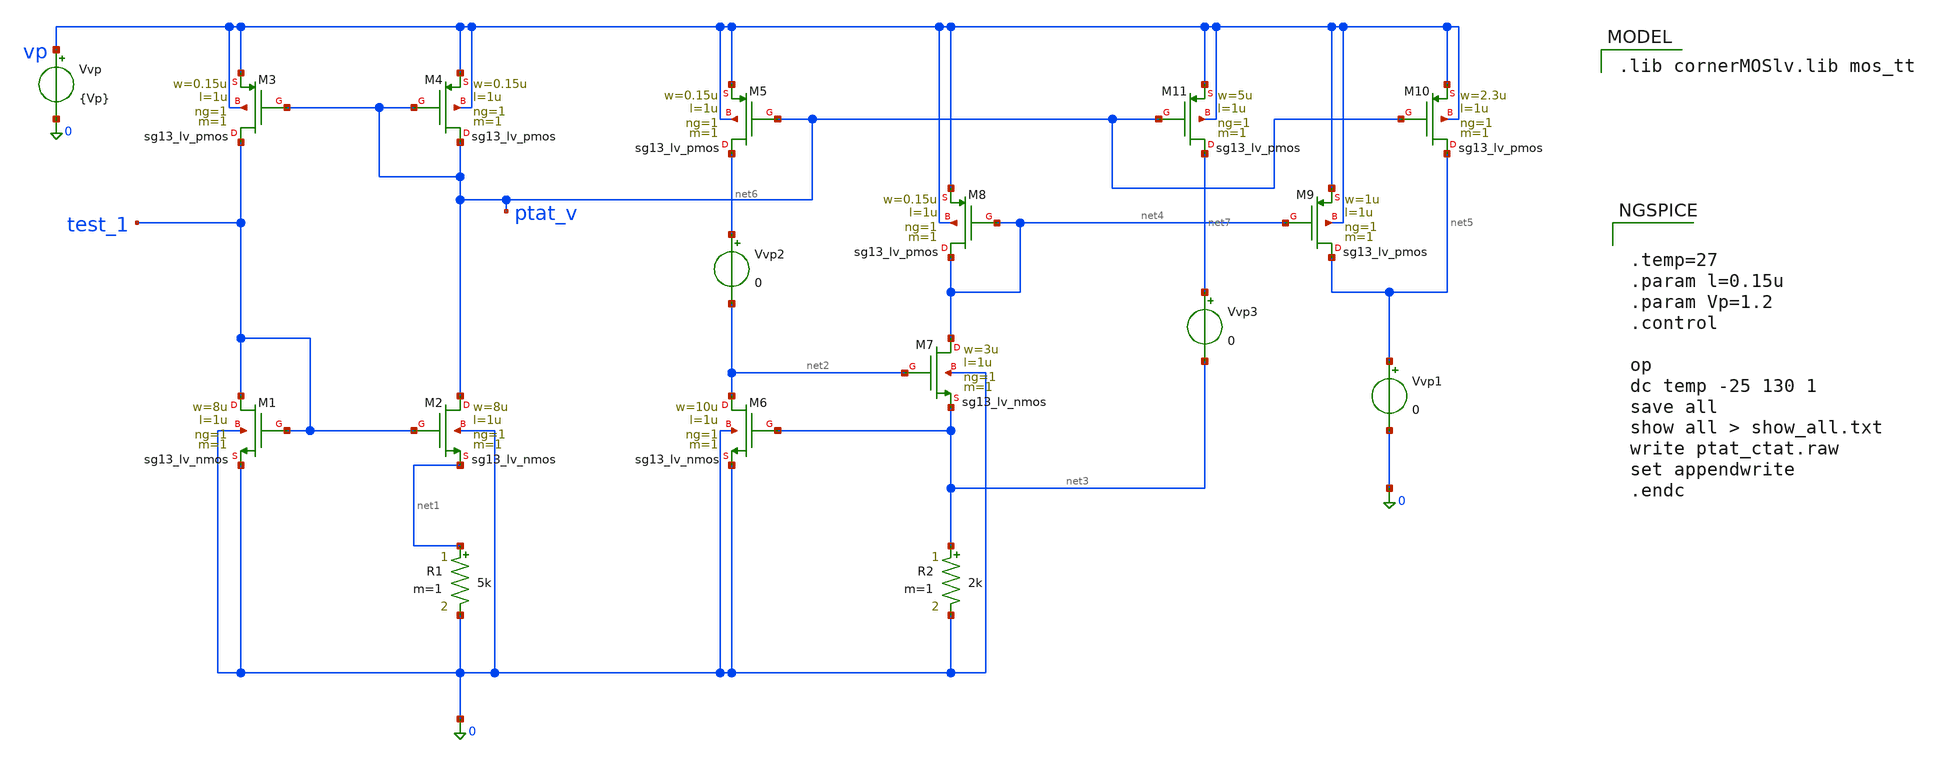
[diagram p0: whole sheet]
** sch_path: schematics/charge_pump/vbias/ptat_ctat.sch
**.subckt ptat_ctat
XM1 test_1 test_1 0 0 sg13_lv_nmos w=8u l=1u ng=1 m=1 mm_ok=1
XM3 test_1 ptat_v vp vp sg13_lv_pmos w=0.15u l=1u ng=1 m=1 mm_ok=1
XM2 ptat_v test_1 net1 0 sg13_lv_nmos w=8u l=1u ng=1 m=1 mm_ok=1
XM4 ptat_v ptat_v vp vp sg13_lv_pmos w=0.15u l=1u ng=1 m=1 mm_ok=1
R1 net1 0 5k m=1
Vvp vp 0 {Vp}
XM6 net2 net3 0 0 sg13_lv_nmos w=10u l=1u ng=1 m=1 mm_ok=1
XM7 net4 net2 net3 0 sg13_lv_nmos w=3u l=1u ng=1 m=1 mm_ok=1
R2 net3 0 2k m=1
XM5 net6 ptat_v vp vp sg13_lv_pmos w=0.15u l=1u ng=1 m=1 mm_ok=1
XM8 net4 net4 vp vp sg13_lv_pmos w=0.15u l=1u ng=1 m=1 mm_ok=1
XM11 net7 ptat_v vp vp sg13_lv_pmos w=5u l=1u ng=1 m=1 mm_ok=1
XM10 net5 ptat_v vp vp sg13_lv_pmos w=2.3u l=1u ng=1 m=1 mm_ok=1
XM9 net5 net4 vp vp sg13_lv_pmos w=1u l=1u ng=1 m=1 mm_ok=1
Vvp1 net5 0 0
.save i(vvp1)
Vvp2 net6 net2 0
Vvp3 net7 net3 0
**** begin user architecture code
 .lib cornerMOSlv.lib mos_tt



.temp=27
.param l=0.15u
.param Vp=1.2
.control

op
dc temp -25 130 1
save all
show all > show_all.txt
write ptat_ctat.raw
set appendwrite
.endc


**** end user architecture code
**.ends
.end
